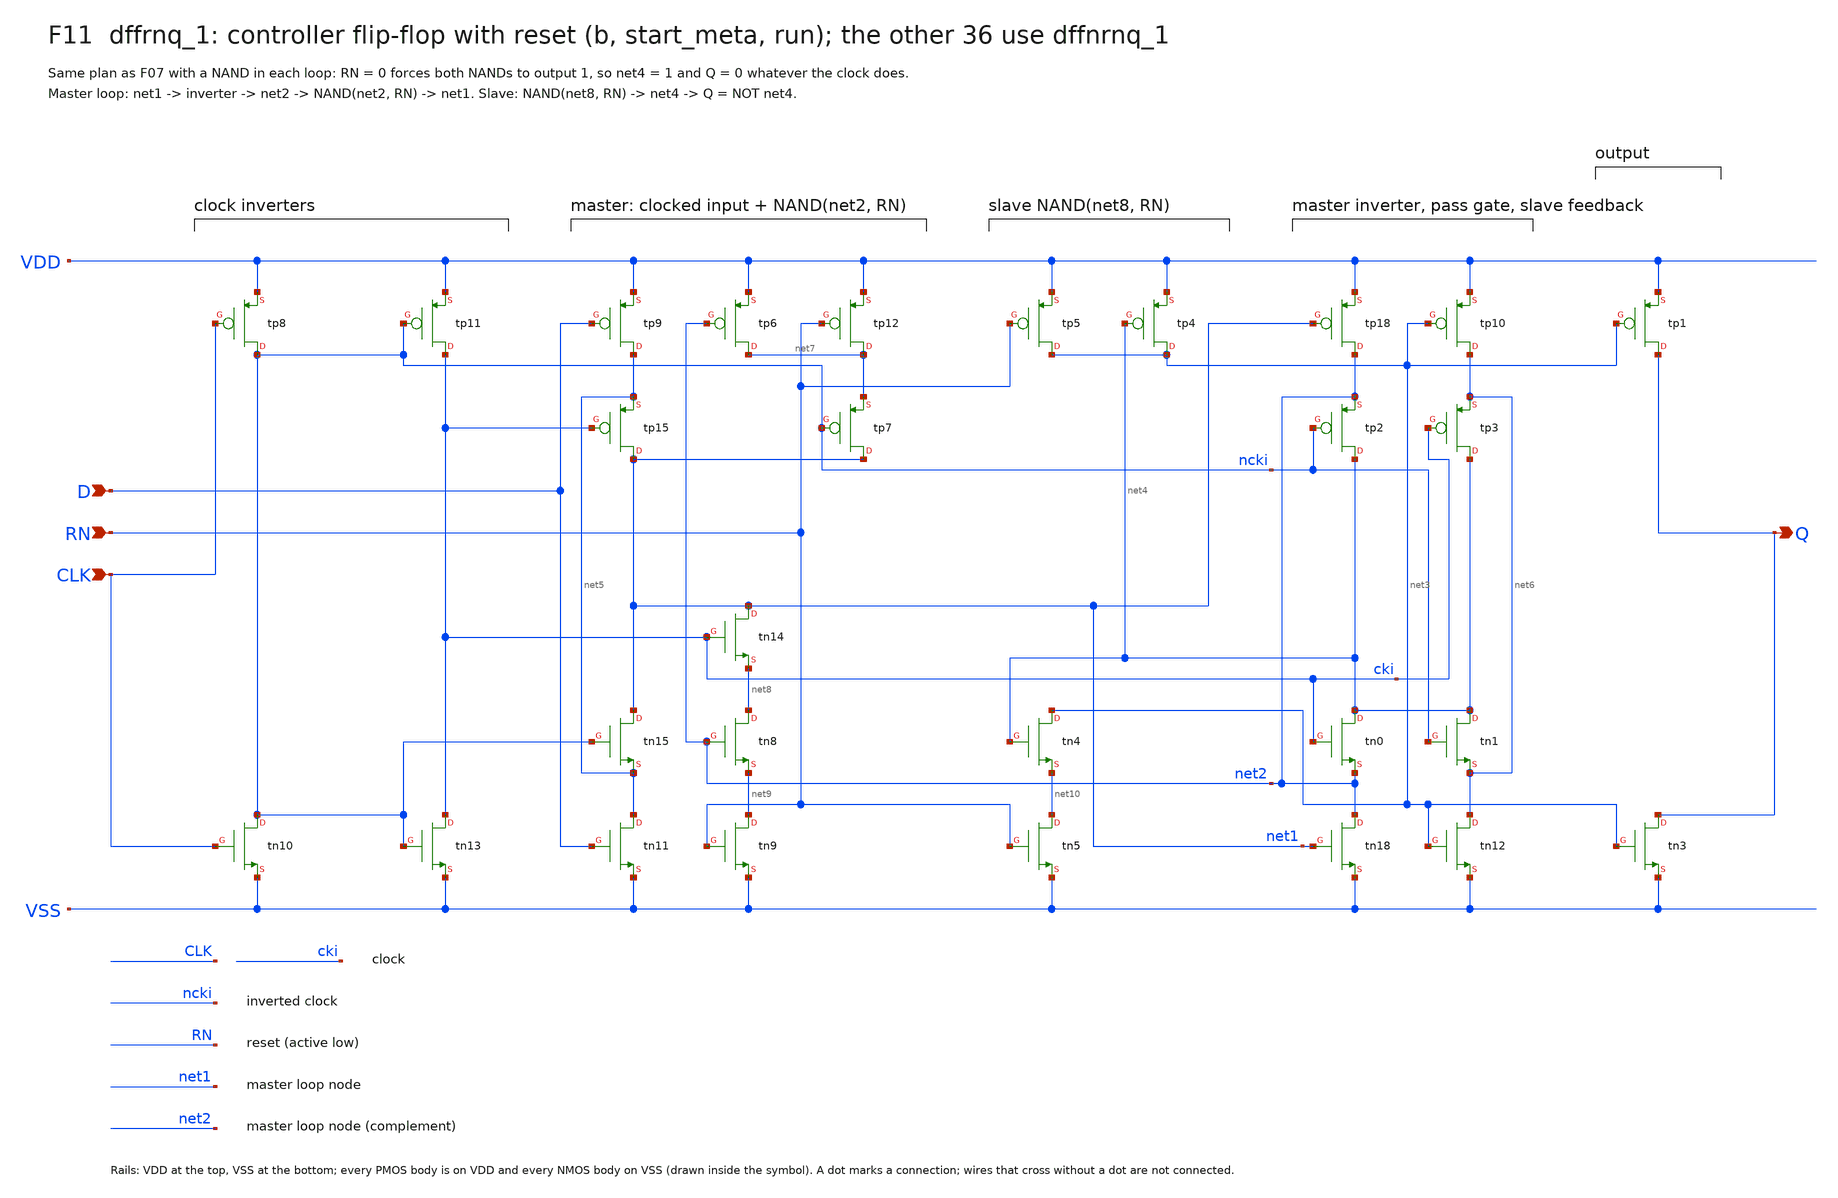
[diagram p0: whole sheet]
** sch_path: xschem/focus/F11_controller_register.sch
**.subckt F11_controller_register D RN CLK Q
*.ipin D
*.ipin RN
*.ipin CLK
*.opin Q
Xtn10 ncki CLK VSS VSS nfet_05v0 L=0.6u W=0.405u nf=1 m=1
Xtn13 cki ncki VSS VSS nfet_05v0 L=0.6u W=0.405u nf=1 m=1
Xtn11 net5 D VSS VSS nfet_05v0 L=0.6u W=0.36u nf=1 m=1
Xtn15 net1 ncki net5 VSS nfet_05v0 L=0.6u W=0.36u nf=1 m=1
Xtn14 net1 cki net8 VSS nfet_05v0 L=0.6u W=0.36u nf=1 m=1
Xtn8 net8 net2 net9 VSS nfet_05v0 L=0.6u W=0.36u nf=1 m=1
Xtn9 net9 RN VSS VSS nfet_05v0 L=0.6u W=0.36u nf=1 m=1
Xtn18 net2 net1 VSS VSS nfet_05v0 L=0.6u W=0.36u nf=1 m=1
Xtn0 net4 cki net2 VSS nfet_05v0 L=0.6u W=0.36u nf=1 m=1
Xtn1 net4 ncki net6 VSS nfet_05v0 L=0.6u W=0.36u nf=1 m=1
Xtn12 net6 net3 VSS VSS nfet_05v0 L=0.6u W=0.36u nf=1 m=1
Xtn5 net10 RN VSS VSS nfet_05v0 L=0.6u W=0.36u nf=1 m=1
Xtn4 net3 net4 net10 VSS nfet_05v0 L=0.6u W=0.4u nf=1 m=1
Xtn3 Q net3 VSS VSS nfet_05v0 L=0.6u W=0.815u nf=1 m=1
Xtp8 ncki CLK VDD VDD pfet_05v0 L=0.5u W=0.865u nf=1 m=1
Xtp11 cki ncki VDD VDD pfet_05v0 L=0.5u W=0.865u nf=1 m=1
Xtp9 net5 D VDD VDD pfet_05v0 L=0.5u W=0.78u nf=1 m=1
Xtp15 net1 cki net5 VDD pfet_05v0 L=0.5u W=0.78u nf=1 m=1
Xtp7 net1 ncki net7 VDD pfet_05v0 L=0.5u W=0.78u nf=1 m=1
Xtp6 net7 net2 VDD VDD pfet_05v0 L=0.5u W=0.78u nf=1 m=1
Xtp12 net7 RN VDD VDD pfet_05v0 L=0.5u W=0.78u nf=1 m=1
Xtp18 net2 net1 VDD VDD pfet_05v0 L=0.5u W=0.505u nf=1 m=1
Xtp2 net4 ncki net2 VDD pfet_05v0 L=0.5u W=0.505u nf=1 m=1
Xtp3 net4 cki net6 VDD pfet_05v0 L=0.5u W=0.505u nf=1 m=1
Xtp10 net6 net3 VDD VDD pfet_05v0 L=0.5u W=0.505u nf=1 m=1
Xtp5 net3 RN VDD VDD pfet_05v0 L=0.5u W=1u nf=1 m=1
Xtp4 net3 net4 VDD VDD pfet_05v0 L=0.5u W=1u nf=1 m=1
Xtp1 Q net3 VDD VDD pfet_05v0 L=0.5u W=1.215u nf=1 m=1
**.ends
.end
